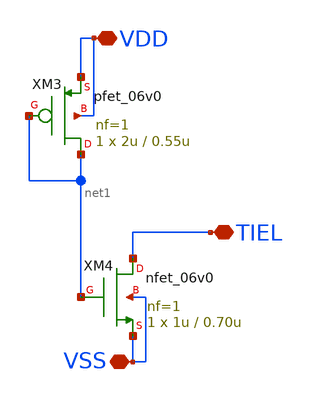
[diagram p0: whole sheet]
** sch_path: blocks/composite/regulated_cascoded_cmirror/xschem/Chipathon2025_pads/xschem/tieL.sch
**.subckt tieL VSS VDD TIEL
*.iopin VSS
*.iopin VDD
*.iopin TIEL
XM3 net1 net1 VDD VDD pfet_06v0 L=0.55u W=2u nf=1 ad='int((nf+1)/2) * W/nf * 0.18u' as='int((nf+2)/2) * W/nf * 0.18u'
+ pd='2*int((nf+1)/2) * (W/nf + 0.18u)' ps='2*int((nf+2)/2) * (W/nf + 0.18u)' nrd='0.18u / W' nrs='0.18u / W'
+ sa=0 sb=0 sd=0 m=1
XM4 TIEL net1 VSS VSS nfet_06v0 L=0.70u W=1u nf=1 ad='int((nf+1)/2) * W/nf * 0.18u' as='int((nf+2)/2) * W/nf * 0.18u'
+ pd='2*int((nf+1)/2) * (W/nf + 0.18u)' ps='2*int((nf+2)/2) * (W/nf + 0.18u)' nrd='0.18u / W' nrs='0.18u / W'
+ sa=0 sb=0 sd=0 m=1
**.ends
.end
